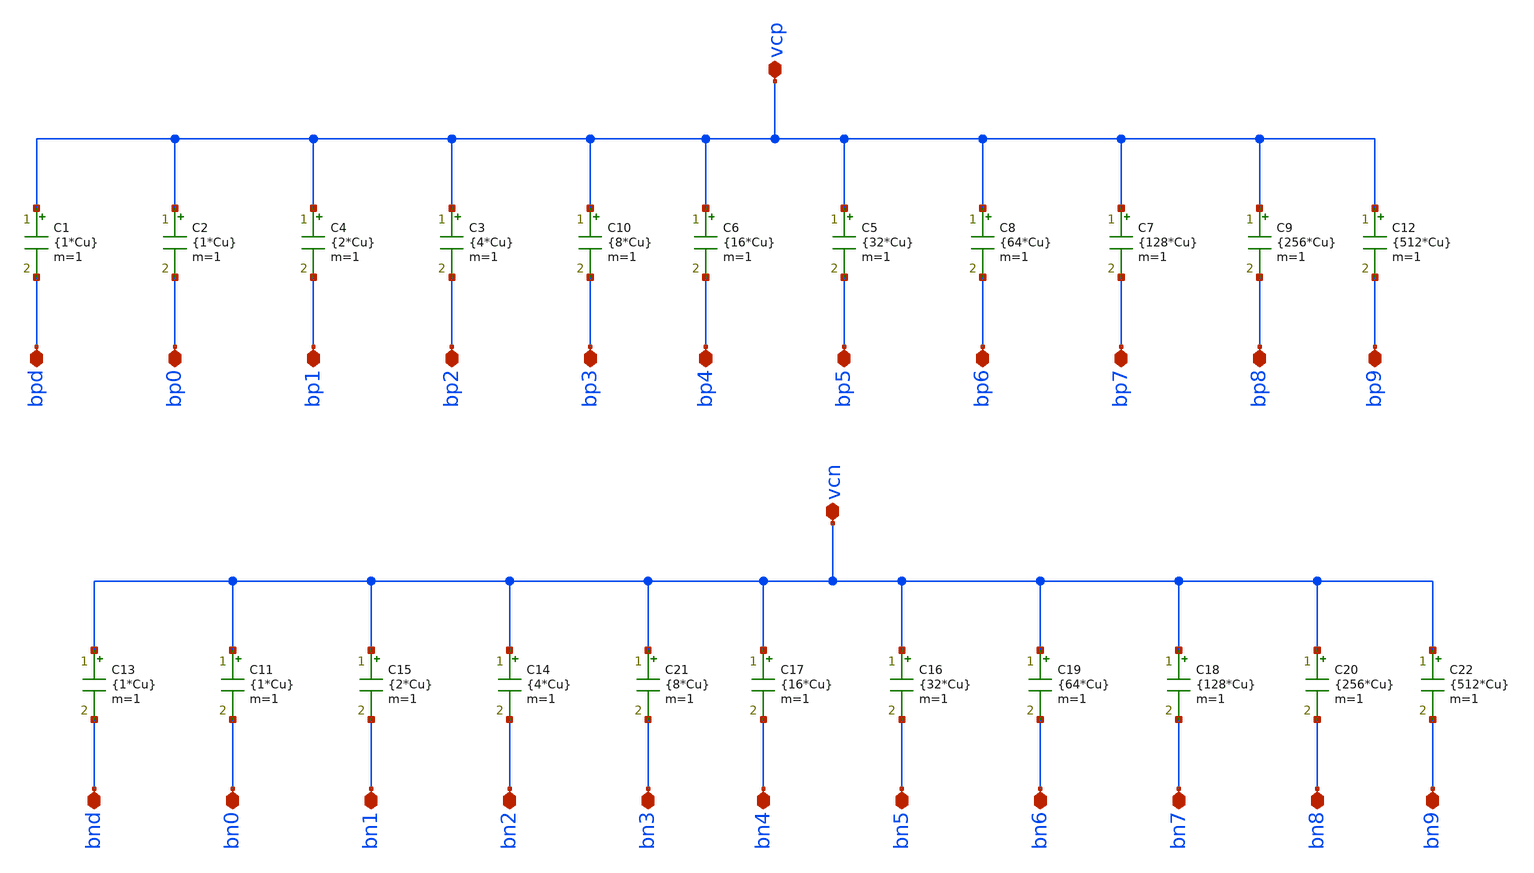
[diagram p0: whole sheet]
** sch_path: circuit_files/sar_adc_test/xschem/cdac_caps_10b_diff_ideal.sch
**.subckt cdac_caps_10b_diff_ideal vcp vcn bpd bp0 bp1 bp2 bp3 bp4 bp5 bp6 bp7 bp8 bp9 bnd bn1 bn2
*+ bn3 bn4 bn5 bn6 bn7 bn8 bn9 bn0
*.iopin vcp
*.iopin vcn
*.iopin bpd
*.iopin bp0
*.iopin bp1
*.iopin bp2
*.iopin bp3
*.iopin bp4
*.iopin bp5
*.iopin bp6
*.iopin bp7
*.iopin bp8
*.iopin bp9
*.iopin bnd
*.iopin bn1
*.iopin bn2
*.iopin bn3
*.iopin bn4
*.iopin bn5
*.iopin bn6
*.iopin bn7
*.iopin bn8
*.iopin bn9
*.iopin bn0
C2 vcp bp0 {1*Cu} m=1
C1 vcp bpd {1*Cu} m=1
C3 vcp bp2 {4*Cu} m=1
C4 vcp bp1 {2*Cu} m=1
C5 vcp bp5 {32*Cu} m=1
C6 vcp bp4 {16*Cu} m=1
C7 vcp bp7 {128*Cu} m=1
C8 vcp bp6 {64*Cu} m=1
C9 vcp bp8 {256*Cu} m=1
C10 vcp bp3 {8*Cu} m=1
C12 vcp bp9 {512*Cu} m=1
C11 vcn bn0 {1*Cu} m=1
C13 vcn bnd {1*Cu} m=1
C14 vcn bn2 {4*Cu} m=1
C15 vcn bn1 {2*Cu} m=1
C16 vcn bn5 {32*Cu} m=1
C17 vcn bn4 {16*Cu} m=1
C18 vcn bn7 {128*Cu} m=1
C19 vcn bn6 {64*Cu} m=1
C20 vcn bn8 {256*Cu} m=1
C21 vcn bn3 {8*Cu} m=1
C22 vcn bn9 {512*Cu} m=1
**** begin user architecture code



.param Cu=5f


**** end user architecture code
**.ends
.end
